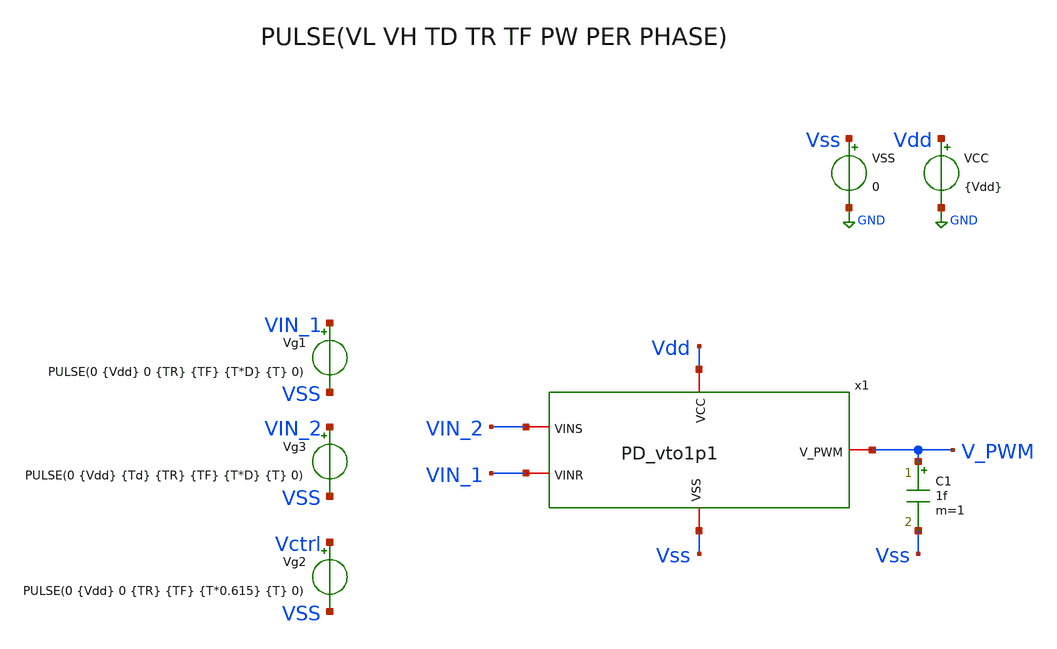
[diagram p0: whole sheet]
** sch_path: ChipUSM_AnalogTrack24/PD/tb_PD_vto1p1.sch
* IHP-GmbH/IHP-Open-PDK/ihp-sg13g2/libs.tech/xschem/sg13g2_stdcells/sg13g2_inv_2.sch:
* Copyright 2023 IHP PDK Authors
* Licensed under the Apache License, Version 2.0 (the "License");
**.subckt tb_PD_vto1p1
VCC Vdd GND {Vdd}
VSS Vss GND 0
Vg1 VIN_1 VSS PULSE(0 {Vdd} 0 {TR} {TF} {T*D} {T} 0)
C1 V_PWM Vss 1f m=1
Vg3 VIN_2 VSS PULSE(0 {Vdd} {Td} {TR} {TF} {T*D} {T} 0)
x1 Vdd Vss VIN_2 V_PWM VIN_1 PD_vto1p1
Vg2 Vctrl VSS PULSE(0 {Vdd} 0 {TR} {TF} {T*0.615} {T} 0)
**** begin user architecture code


.param corner=0

.if (corner==0)
.lib $::SG13G2_MODELS/cornerMOSlv.lib mos_tt
.lib $::SG13G2_MODELS/cornerMOSlv.lib mos_tt
.lib $::SG13G2_MODELS/cornerRES.lib res_typ
.lib $::SG13G2_MODELS/cornerCAP.lib cap_typ
.endif

.include /opt/pdks/ihp-sg13g2/libs.ref/sg13g2_stdcell/spice/sg13g2_stdcell.spice



.param Vdd = 1.2
.param VH = 3.3
.param Del = 0

.param T = 0.1u
.param TR = 1p
.param TF = 1p
.param DD = 0.615

*Caso 1 - No funciona bien
*.param D = 0.8
*.param Td = 0.03u

*Caso 2 - Funciona bien
.param D = 0.5
.param Td = DD*T

*Caso 3 - Funciona bien
*.param D = 0.615
*.param Td = 0.03u

*Caso 4 - No funciona bien
*.param D = 0.615
*.param Td = 0.08u




.param temp = 27





.save all

.control
set color0 = white
tran 100p 300n
plot v(VIN_1) v(VIN_2)+1.5 v(V_PWM)+3
plot v(V_PWM) v(Vctrl)+1.5
.endc

*.measure tran tdead_fall
*+ TRIG tran1.V(vcn) TD=0u VAL=0.6 FALL=1
*+ TARG tran1.V(vcp) TD=0u VAL=0.6 FALL=1

*.measure tran t_large_delay
*+ TRIG tran1.V(x1.C1) TD=0u VAL=0.6 RISE=1
*+ TARG tran1.V(x1.B2) TD=0u VAL=0.6 RISE=1



**** end user architecture code
**.ends

* expanding   symbol:  PD_vto1p1.sym # of pins=5
** sym_path: PD_vto1p1.sym
** sch_path: PD_vto1p1.sch
.subckt PD_vto1p1 VCC VSS VINS V_PWM VINR
*.iopin V_PWM
*.iopin VCC
*.iopin VSS
*.iopin VINS
*.iopin VINR
x3 V_N net2 V_PWM VCC VSS sg13g2_nor2_1
x1 V_PWM V_N net1 VCC VSS sg13g2_nor2_1
C2 VFE1 VSS 100f m=1
C1 VFE1 VSS 100f m=1
x4 VCC VSS VFE1 VINR net2 SPG_vto1p1
x2 VCC VSS VFE1 VINS net1 SPG_vto1p1
.ends


* expanding   symbol:  sg13g2_stdcells/sg13g2_nor2_1.sym # of pins=3
** sym_path: sg13g2_stdcells/sg13g2_nor2_1.sym
** sch_path: sg13g2_stdcells/sg13g2_nor2_1.sch
.subckt sg13g2_nor2_1 Y A B VDD VSS
*.opin Y
*.ipin B
*.ipin A
*.iopin VDD
*.iopin VSS
XM1 Y A VSS VSS sg13_lv_nmos w=740.00n l=130.00n ng=1 m=1 mm_ok=1
XM2 Y B VSS VSS sg13_lv_nmos w=740.00n l=130.00n ng=1 m=1 mm_ok=1
XM3 net1 A VDD VDD sg13_lv_pmos w=1.12u l=130.00n ng=1 m=1 mm_ok=1
XM4 Y B net1 VDD sg13_lv_pmos w=1.12u l=130.00n ng=1 m=1 mm_ok=1
.ends


* expanding   symbol:  ../SPG/SPG_vto1p1.sym # of pins=5
** sym_path: ../SPG/SPG_vto1p1.sym
** sch_path: ../SPG/SPG_vto1p1.sch
.subckt SPG_vto1p1 VCC VSS VFE VIN VRE
*.iopin VIN
*.iopin VFE
*.iopin VRE
*.iopin VCC
*.iopin VSS
x1 dly8 dly7 VCC VSS sg13g2_inv_1
x2 net2 predly VCC VSS sg13g2_inv_1
x3 predly net3 VCC VSS sg13g2_inv_1
x4 net1 dly8 VCC VSS sg13g2_inv_1
x5 net3 VIN VCC VSS sg13g2_inv_2
x6 V_gatein predly VCC VSS sg13g2_inv_8
x7 VFE net2 dly8 VCC VSS sg13g2_and2_2
x8 VRE net1 predly VCC VSS sg13g2_and2_2
x9 VCC VSS V_gatein dly7 large_delay_vto1p1
.ends


* expanding   symbol:  sg13g2_stdcells/sg13g2_inv_1.sym # of pins=2
** sym_path: sg13g2_stdcells/sg13g2_inv_1.sym
** sch_path: sg13g2_stdcells/sg13g2_inv_1.sch
.subckt sg13g2_inv_1 Y A VDD VSS
*.opin Y
*.ipin A
*.iopin VDD
*.iopin VSS
XM1 Y A VSS VSS sg13_lv_nmos w=740.00n l=130.00n ng=1 m=1 mm_ok=1
XM2 Y A VDD VDD sg13_lv_pmos w=1.12u l=130.00n ng=1 m=1 mm_ok=1
.ends


* expanding   symbol:  sg13g2_stdcells/sg13g2_inv_2.sym # of pins=2
** sym_path: sg13g2_stdcells/sg13g2_inv_2.sym
** sch_path: sg13g2_stdcells/sg13g2_inv_2.sch
.subckt sg13g2_inv_2 Y A VDD VSS
*.opin Y
*.ipin A
*.iopin VDD
*.iopin VSS
XM1 Y A VSS VSS sg13_lv_nmos w=1.48u l=130.00n ng=2 m=1 mm_ok=1
XM2 Y A VDD VDD sg13_lv_pmos w=2.24u l=130.00n ng=2 m=1 mm_ok=1
.ends


* expanding   symbol:  sg13g2_stdcells/sg13g2_inv_8.sym # of pins=2
** sym_path: sg13g2_stdcells/sg13g2_inv_8.sym
** sch_path: sg13g2_stdcells/sg13g2_inv_8.sch
.subckt sg13g2_inv_8 Y A VDD VSS
*.opin Y
*.ipin A
*.iopin VDD
*.iopin VSS
XM1 Y A VSS VSS sg13_lv_nmos w=5.92u l=130.00n ng=8 m=1 mm_ok=1
XM2 Y A VDD VDD sg13_lv_pmos w=8.96u l=130.00n ng=8 m=1 mm_ok=1
.ends


* expanding   symbol:  sg13g2_stdcells/sg13g2_and2_2.sym # of pins=3
** sym_path: sg13g2_stdcells/sg13g2_and2_2.sym
** sch_path: sg13g2_stdcells/sg13g2_and2_2.sch
.subckt sg13g2_and2_2 X A B VDD VSS
*.ipin A
*.ipin B
*.opin X
*.iopin VDD
*.iopin VSS
XM1 net1 A net2 VSS sg13_lv_nmos w=640.00n l=130.00n ng=1 m=1 mm_ok=1
XM2 net2 B VSS VSS sg13_lv_nmos w=640.00n l=130.00n ng=1 m=1 mm_ok=1
XM3 X net1 VSS VSS sg13_lv_nmos w=1.48u l=130.00n ng=2 m=1 mm_ok=1
XM4 net1 B VDD VDD sg13_lv_pmos w=840.00n l=130.00n ng=1 m=1 mm_ok=1
XM5 net1 A VDD VDD sg13_lv_pmos w=840.00n l=130.00n ng=1 m=1 mm_ok=1
XM6 X net1 VDD VDD sg13_lv_pmos w=2.24u l=130.00n ng=2 m=1 mm_ok=1
.ends


* expanding   symbol:  ../large_delay/large_delay_vto1p1.sym # of pins=4
** sym_path: ../large_delay/large_delay_vto1p1.sym
** sch_path: ../large_delay/large_delay_vto1p1.sch
.subckt large_delay_vto1p1 VCC VSS VIN VOUT
*.iopin VIN
*.iopin VOUT
*.iopin VCC
*.iopin VSS
x1[0] n2 VIN VCC VSS sg13g2_dlygate4sd3_1
x1[1] n3 n2 VCC VSS sg13g2_dlygate4sd3_1
x1[2] n4 n3 VCC VSS sg13g2_dlygate4sd3_1
x1[3] n5 n4 VCC VSS sg13g2_dlygate4sd3_1
x1[4] VOUT n5 VCC VSS sg13g2_dlygate4sd3_1
.ends


* expanding   symbol:  sg13g2_stdcells/sg13g2_dlygate4sd3_1.sym # of pins=2
** sym_path: sg13g2_stdcells/sg13g2_dlygate4sd3_1.sym
** sch_path: sg13g2_stdcells/sg13g2_dlygate4sd3_1.sch
.subckt sg13g2_dlygate4sd3_1 X A VDD VSS
*.ipin A
*.opin X
*.iopin VDD
*.iopin VSS
XM1 net3 A VSS VSS sg13_lv_nmos w=420.00n l=130.00n ng=1 m=1 mm_ok=1
XM2 net1 net3 VSS VSS sg13_lv_nmos w=420.00n l=500.0n ng=1 m=1 mm_ok=1
XM3 net2 net1 VSS VSS sg13_lv_nmos w=420.00n l=500.0n ng=1 m=1 mm_ok=1
XM4 X net2 VSS VSS sg13_lv_nmos w=740.00n l=130.00n ng=1 m=1 mm_ok=1
XM5 net3 A VDD VDD sg13_lv_pmos w=420.00n l=130.00n ng=1 m=1 mm_ok=1
XM6 net1 net3 VDD VDD sg13_lv_pmos w=1.000u l=500.0n ng=1 m=1 mm_ok=1
XM7 net2 net1 VDD VDD sg13_lv_pmos w=1.000u l=500.0n ng=1 m=1 mm_ok=1
XM8 X net2 VDD VDD sg13_lv_pmos w=1.12u l=130.00n ng=1 m=1 mm_ok=1
.ends

.GLOBAL GND
.end
